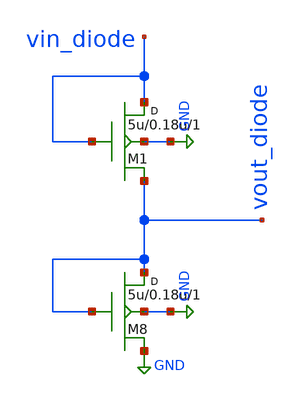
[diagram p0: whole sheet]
** sch_path: synthetic/blocks/diode_connected_nmos.sch
**.subckt diode_connected_nmos
M8 vout_diode vout_diode GND GND nmos w=5u l=0.18u m=1
M1 vin_diode vin_diode vout_diode GND nmos w=5u l=0.18u m=1
**.ends
.GLOBAL GND
.end
